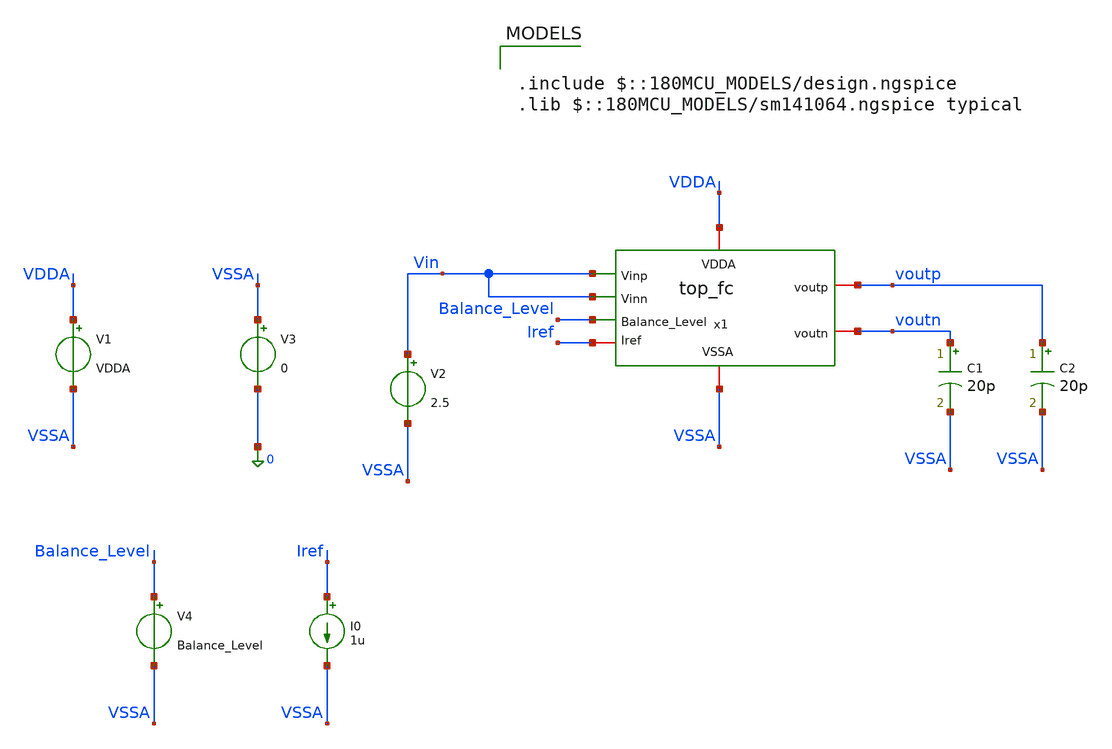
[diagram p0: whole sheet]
** sch_path: Folded_cascode/testbenches/top_fc_op_tb.sch
**.subckt top_fc_op_tb
x1 Balance_Level Vin voutp VDDA voutn Vin Iref VSSA top_fc
V2 Vin VSSA 2.5
C1 voutn VSSA 20p m=1
C2 voutp VSSA 20p m=1
V1 VDDA VSSA VDDA
V3 VSSA 0 0
V4 Balance_Level VSSA Balance_Level
I0 Iref VSSA 1u
**** begin user architecture code

.include $::180MCU_MODELS/design.ngspice
.lib $::180MCU_MODELS/sm141064.ngspice typical



.temp 27
.param VDDA = 5
.param Balance_Level = 1.5

.control
option sparse
set filetype=ascii
set wr_singlescale
set wr_vecnames
save all
save @m.x1.x1.xm1.m0[id]
save @m.x1.x1.xm1.m0[gm]
save @m.x1.x1.xm1.m0[vgs]
save @m.x1.x1.xm1.m0[vds]
save @m.x1.x1.xm1.m0[vth]
save @m.x1.x1.xm1.m0[gds]
save @m.x1.x1.xm1.m0[vdsat]

save @m.x1.x1.xm2.m0[id]
save @m.x1.x1.xm2.m0[gm]
save @m.x1.x1.xm2.m0[vgs]
save @m.x1.x1.xm2.m0[vds]
save @m.x1.x1.xm2.m0[vth]
save @m.x1.x1.xm2.m0[gds]
save @m.x1.x1.xm2.m0[vdsat]

save @m.x1.x1.xm9.m0[id]
save @m.x1.x1.xm9.m0[gm]
save @m.x1.x1.xm9.m0[vgs]
save @m.x1.x1.xm9.m0[vds]
save @m.x1.x1.xm9.m0[vth]
save @m.x1.x1.xm9.m0[gds]
save @m.x1.x1.xm9.m0[vdsat]

save @m.x1.x1.xm8.m0[id]
save @m.x1.x1.xm8.m0[gm]
save @m.x1.x1.xm8.m0[vgs]
save @m.x1.x1.xm8.m0[vds]
save @m.x1.x1.xm8.m0[vth]
save @m.x1.x1.xm8.m0[gds]
save @m.x1.x1.xm8.m0[vdsat]

save @m.x1.x1.xm6.m0[id]
save @m.x1.x1.xm6.m0[gm]
save @m.x1.x1.xm6.m0[vgs]
save @m.x1.x1.xm6.m0[vds]
save @m.x1.x1.xm6.m0[vth]
save @m.x1.x1.xm6.m0[gds]
save @m.x1.x1.xm6.m0[vdsat]

save @m.x1.x1.xm5.m0[id]
save @m.x1.x1.xm5.m0[gm]
save @m.x1.x1.xm5.m0[vgs]
save @m.x1.x1.xm5.m0[vds]
save @m.x1.x1.xm5.m0[vth]
save @m.x1.x1.xm5.m0[gds]
save @m.x1.x1.xm5.m0[vdsat]

save @m.x1.x2.xm1.m0[id]
save @m.x1.x2.xm1.m0[gm]
save @m.x1.x2.xm1.m0[vgs]
save @m.x1.x2.xm1.m0[vds]
save @m.x1.x2.xm1.m0[vth]
save @m.x1.x2.xm1.m0[gds]

save @m.x1.x2.xm2.m0[id]
save @m.x1.x2.xm2.m0[gm]
save @m.x1.x2.xm2.m0[vgs]
save @m.x1.x2.xm2.m0[vds]
save @m.x1.x2.xm2.m0[vth]
save @m.x1.x2.xm2.m0[gds]

save @m.x1.x2.xm3.m0[id]
save @m.x1.x2.xm3.m0[gm]
save @m.x1.x2.xm3.m0[vgs]
save @m.x1.x2.xm3.m0[vds]
save @m.x1.x2.xm3.m0[vth]
save @m.x1.x2.xm3.m0[gds]

save @m.x1.x2.xm4.m0[id]
save @m.x1.x2.xm4.m0[gm]
save @m.x1.x2.xm4.m0[vgs]
save @m.x1.x2.xm4.m0[vds]
save @m.x1.x2.xm4.m0[vth]
save @m.x1.x2.xm4.m0[gds]

save @m.x1.x2.xm5.m0[id]
save @m.x1.x2.xm5.m0[gm]
save @m.x1.x2.xm5.m0[vgs]
save @m.x1.x2.xm5.m0[vds]
save @m.x1.x2.xm5.m0[vth]
save @m.x1.x2.xm5.m0[gds]

save @m.x1.x2.xm6.m0[id]
save @m.x1.x2.xm6.m0[gm]
save @m.x1.x2.xm6.m0[vgs]
save @m.x1.x2.xm6.m0[vds]
save @m.x1.x2.xm6.m0[vth]
save @m.x1.x2.xm6.m0[gds]

save @m.x1.x2.xm7.m0[id]
save @m.x1.x2.xm7.m0[gm]
save @m.x1.x2.xm7.m0[vgs]
save @m.x1.x2.xm7.m0[vds]
save @m.x1.x2.xm7.m0[vth]
save @m.x1.x2.xm7.m0[gds]

save @m.x1.x2.xm8.m0[id]
save @m.x1.x2.xm8.m0[gm]
save @m.x1.x2.xm8.m0[vgs]
save @m.x1.x2.xm8.m0[vds]
save @m.x1.x2.xm8.m0[vth]
save @m.x1.x2.xm8.m0[gds]

save @m.x1.x2.xm9.m0[id]
save @m.x1.x2.xm9.m0[gm]
save @m.x1.x2.xm9.m0[vgs]
save @m.x1.x2.xm9.m0[vds]
save @m.x1.x2.xm9.m0[vth]
save @m.x1.x2.xm9.m0[gds]

save @m.x1.x3.xm1.m0[id]
save @m.x1.x3.xm1.m0[gm]
save @m.x1.x3.xm1.m0[vgs]
save @m.x1.x3.xm1.m0[vds]
save @m.x1.x3.xm1.m0[vth]
save @m.x1.x3.xm1.m0[gds]

save @m.x1.x3.xm2.m0[id]
save @m.x1.x3.xm2.m0[gm]
save @m.x1.x3.xm2.m0[vgs]
save @m.x1.x3.xm2.m0[vds]
save @m.x1.x3.xm2.m0[vth]
save @m.x1.x3.xm2.m0[gds]

save @m.x1.x3.xm3.m0[id]
save @m.x1.x3.xm3.m0[gm]
save @m.x1.x3.xm3.m0[vgs]
save @m.x1.x3.xm3.m0[vds]
save @m.x1.x3.xm3.m0[vth]
save @m.x1.x3.xm3.m0[gds]

save @m.x1.x3.xm4.m0[id]
save @m.x1.x3.xm4.m0[gm]
save @m.x1.x3.xm4.m0[vgs]
save @m.x1.x3.xm4.m0[vds]
save @m.x1.x3.xm4.m0[vth]
save @m.x1.x3.xm4.m0[gds]

save @m.x1.x3.xm5.m0[id]
save @m.x1.x3.xm5.m0[gm]
save @m.x1.x3.xm5.m0[vgs]
save @m.x1.x3.xm5.m0[vds]
save @m.x1.x3.xm5.m0[vth]
save @m.x1.x3.xm5.m0[gds]

save @m.x1.x3.xm6.m0[id]
save @m.x1.x3.xm6.m0[gm]
save @m.x1.x3.xm6.m0[vgs]
save @m.x1.x3.xm6.m0[vds]
save @m.x1.x3.xm6.m0[vth]
save @m.x1.x3.xm6.m0[gds]

save @m.x1.x3.xm7.m0[id]
save @m.x1.x3.xm7.m0[gm]
save @m.x1.x3.xm7.m0[vgs]
save @m.x1.x3.xm7.m0[vds]
save @m.x1.x3.xm7.m0[vth]
save @m.x1.x3.xm7.m0[gds]

save @m.x1.x3.xm8.m0[id]
save @m.x1.x3.xm8.m0[gm]
save @m.x1.x3.xm8.m0[vgs]
save @m.x1.x3.xm8.m0[vds]
save @m.x1.x3.xm8.m0[vth]
save @m.x1.x3.xm8.m0[gds]

save @m.x1.x3.xm9.m0[id]
save @m.x1.x3.xm9.m0[gm]
save @m.x1.x3.xm9.m0[vgs]
save @m.x1.x3.xm9.m0[vds]
save @m.x1.x3.xm9.m0[vth]
save @m.x1.x3.xm9.m0[gds]

save @m.x1.x3.xm10.m0[id]
save @m.x1.x3.xm10.m0[gm]
save @m.x1.x3.xm10.m0[vgs]
save @m.x1.x3.xm10.m0[vds]
save @m.x1.x3.xm10.m0[vth]
save @m.x1.x3.xm10.m0[gds]

save @m.x1.x3.xm11.m0[id]
save @m.x1.x3.xm11.m0[gm]
save @m.x1.x3.xm11.m0[vgs]
save @m.x1.x3.xm11.m0[vds]
save @m.x1.x3.xm11.m0[vth]
save @m.x1.x3.xm11.m0[gds]

save @m.x1.x3.xm12.m0[id]
save @m.x1.x3.xm12.m0[gm]
save @m.x1.x3.xm12.m0[vgs]
save @m.x1.x3.xm12.m0[vds]
save @m.x1.x3.xm12.m0[vth]
save @m.x1.x3.xm12.m0[gds]

save @m.x1.x3.xm13.m0[id]
save @m.x1.x3.xm13.m0[gm]
save @m.x1.x3.xm13.m0[vgs]
save @m.x1.x3.xm13.m0[vds]
save @m.x1.x3.xm13.m0[vth]
save @m.x1.x3.xm13.m0[gds]

save @m.x1.x3.xm14.m0[id]
save @m.x1.x3.xm14.m0[gm]
save @m.x1.x3.xm14.m0[vgs]
save @m.x1.x3.xm14.m0[vds]
save @m.x1.x3.xm14.m0[vth]
save @m.x1.x3.xm14.m0[gds]

save @m.x1.x3.xm15.m0[id]
save @m.x1.x3.xm15.m0[gm]
save @m.x1.x3.xm15.m0[vgs]
save @m.x1.x3.xm15.m0[vds]
save @m.x1.x3.xm15.m0[vth]
save @m.x1.x3.xm15.m0[gds]

save @m.x1.x3.xm16.m0[id]
save @m.x1.x3.xm16.m0[gm]
save @m.x1.x3.xm16.m0[vgs]
save @m.x1.x3.xm16.m0[vds]
save @m.x1.x3.xm16.m0[vth]
save @m.x1.x3.xm16.m0[gds]

save @m.x1.x3.xm17.m0[id]
save @m.x1.x3.xm17.m0[gm]
save @m.x1.x3.xm17.m0[vgs]
save @m.x1.x3.xm17.m0[vds]
save @m.x1.x3.xm17.m0[vth]
save @m.x1.x3.xm17.m0[gds]

save @m.x1.x3.xm18.m0[id]
save @m.x1.x3.xm18.m0[gm]
save @m.x1.x3.xm18.m0[vgs]
save @m.x1.x3.xm18.m0[vds]
save @m.x1.x3.xm18.m0[vth]
save @m.x1.x3.xm18.m0[gds]

save @m.x1.x3.xm21.m0[id]
save @m.x1.x3.xm21.m0[gm]
save @m.x1.x3.xm21.m0[vgs]
save @m.x1.x3.xm21.m0[vds]
save @m.x1.x3.xm21.m0[vth]
save @m.x1.x3.xm21.m0[gds]

save @m.x1.x3.xm22.m0[id]
save @m.x1.x3.xm22.m0[gm]
save @m.x1.x3.xm22.m0[vgs]
save @m.x1.x3.xm22.m0[vds]
save @m.x1.x3.xm22.m0[vth]
save @m.x1.x3.xm22.m0[gds]

op
write top_fc_op_tb.raw all

.endc


**** end user architecture code
**.ends
.end
